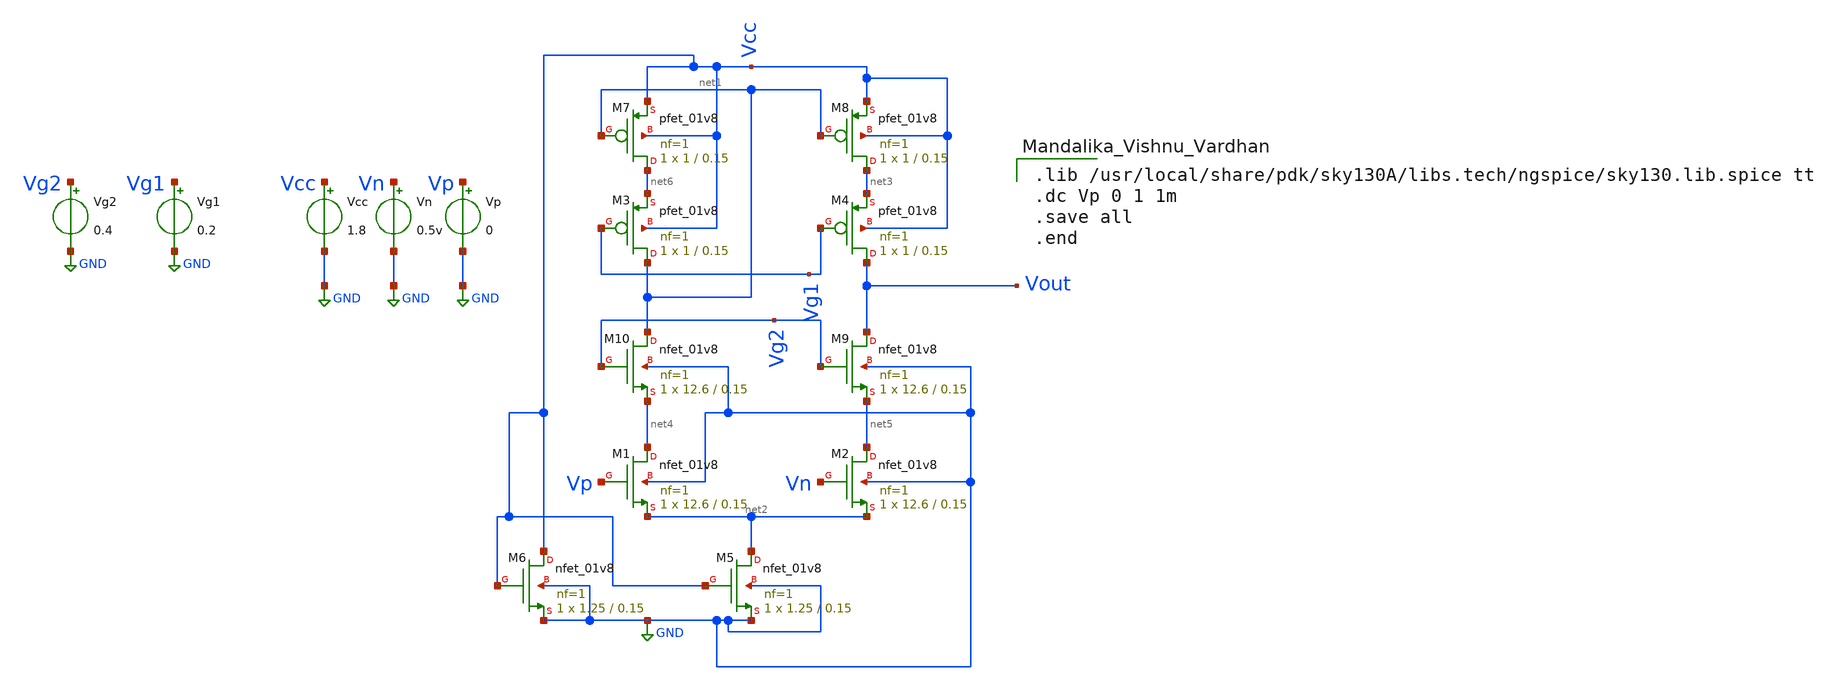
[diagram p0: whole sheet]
** sch_path: TelescopicOpAmp.sch
**.subckt TelescopicOpAmp
XM1 net4 Vp net2 GND sky130_fd_pr__nfet_01v8 L=0.15 W=12.6 nf=1 ad='int((nf+1)/2) * W/nf * 0.29' as='int((nf+2)/2) * W/nf * 0.29'
+ pd='2*int((nf+1)/2) * (W/nf + 0.29)' ps='2*int((nf+2)/2) * (W/nf + 0.29)' nrd='0.29 / W' nrs='0.29 / W'
+ sa=0 sb=0 sd=0 mult=1 m=1
XM2 net5 Vn net2 GND sky130_fd_pr__nfet_01v8 L=0.15 W=12.6 nf=1 ad='int((nf+1)/2) * W/nf * 0.29' as='int((nf+2)/2) * W/nf * 0.29'
+ pd='2*int((nf+1)/2) * (W/nf + 0.29)' ps='2*int((nf+2)/2) * (W/nf + 0.29)' nrd='0.29 / W' nrs='0.29 / W'
+ sa=0 sb=0 sd=0 mult=1 m=1
XM3 net1 Vg1 net6 Vcc sky130_fd_pr__pfet_01v8 L=0.15 W=1 nf=1 ad='int((nf+1)/2) * W/nf * 0.29' as='int((nf+2)/2) * W/nf * 0.29'
+ pd='2*int((nf+1)/2) * (W/nf + 0.29)' ps='2*int((nf+2)/2) * (W/nf + 0.29)' nrd='0.29 / W' nrs='0.29 / W'
+ sa=0 sb=0 sd=0 mult=1 m=1
XM4 Vout Vg1 net3 Vcc sky130_fd_pr__pfet_01v8 L=0.15 W=1 nf=1 ad='int((nf+1)/2) * W/nf * 0.29' as='int((nf+2)/2) * W/nf * 0.29'
+ pd='2*int((nf+1)/2) * (W/nf + 0.29)' ps='2*int((nf+2)/2) * (W/nf + 0.29)' nrd='0.29 / W' nrs='0.29 / W'
+ sa=0 sb=0 sd=0 mult=1 m=1
XM5 net2 Vcc GND GND sky130_fd_pr__nfet_01v8 L=0.15 W=1.25 nf=1 ad='int((nf+1)/2) * W/nf * 0.29' as='int((nf+2)/2) * W/nf * 0.29'
+ pd='2*int((nf+1)/2) * (W/nf + 0.29)' ps='2*int((nf+2)/2) * (W/nf + 0.29)' nrd='0.29 / W' nrs='0.29 / W'
+ sa=0 sb=0 sd=0 mult=1 m=1
Vcc Vcc GND 1.8
Vn Vn GND 0.5v
Vp Vp GND 0
XM6 Vcc Vcc GND GND sky130_fd_pr__nfet_01v8 L=0.15 W=1.25 nf=1 ad='int((nf+1)/2) * W/nf * 0.29' as='int((nf+2)/2) * W/nf * 0.29'
+ pd='2*int((nf+1)/2) * (W/nf + 0.29)' ps='2*int((nf+2)/2) * (W/nf + 0.29)' nrd='0.29 / W' nrs='0.29 / W'
+ sa=0 sb=0 sd=0 mult=1 m=1
XM7 net6 net1 Vcc Vcc sky130_fd_pr__pfet_01v8 L=0.15 W=1 nf=1 ad='int((nf+1)/2) * W/nf * 0.29' as='int((nf+2)/2) * W/nf * 0.29'
+ pd='2*int((nf+1)/2) * (W/nf + 0.29)' ps='2*int((nf+2)/2) * (W/nf + 0.29)' nrd='0.29 / W' nrs='0.29 / W'
+ sa=0 sb=0 sd=0 mult=1 m=1
XM8 net3 net1 Vcc Vcc sky130_fd_pr__pfet_01v8 L=0.15 W=1 nf=1 ad='int((nf+1)/2) * W/nf * 0.29' as='int((nf+2)/2) * W/nf * 0.29'
+ pd='2*int((nf+1)/2) * (W/nf + 0.29)' ps='2*int((nf+2)/2) * (W/nf + 0.29)' nrd='0.29 / W' nrs='0.29 / W'
+ sa=0 sb=0 sd=0 mult=1 m=1
XM9 Vout Vg2 net5 GND sky130_fd_pr__nfet_01v8 L=0.15 W=12.6 nf=1 ad='int((nf+1)/2) * W/nf * 0.29' as='int((nf+2)/2) * W/nf * 0.29'
+ pd='2*int((nf+1)/2) * (W/nf + 0.29)' ps='2*int((nf+2)/2) * (W/nf + 0.29)' nrd='0.29 / W' nrs='0.29 / W'
+ sa=0 sb=0 sd=0 mult=1 m=1
XM10 net1 Vg2 net4 GND sky130_fd_pr__nfet_01v8 L=0.15 W=12.6 nf=1 ad='int((nf+1)/2) * W/nf * 0.29' as='int((nf+2)/2) * W/nf * 0.29'
+ pd='2*int((nf+1)/2) * (W/nf + 0.29)' ps='2*int((nf+2)/2) * (W/nf + 0.29)' nrd='0.29 / W' nrs='0.29 / W'
+ sa=0 sb=0 sd=0 mult=1 m=1
Vg1 Vg1 GND 0.2
Vg2 Vg2 GND 0.4
**** begin user architecture code

.lib /usr/local/share/pdk/sky130A/libs.tech/ngspice/sky130.lib.spice tt
.dc Vp 0 1 1m
.save all
.end

**** end user architecture code
**.ends
.GLOBAL GND
.end
